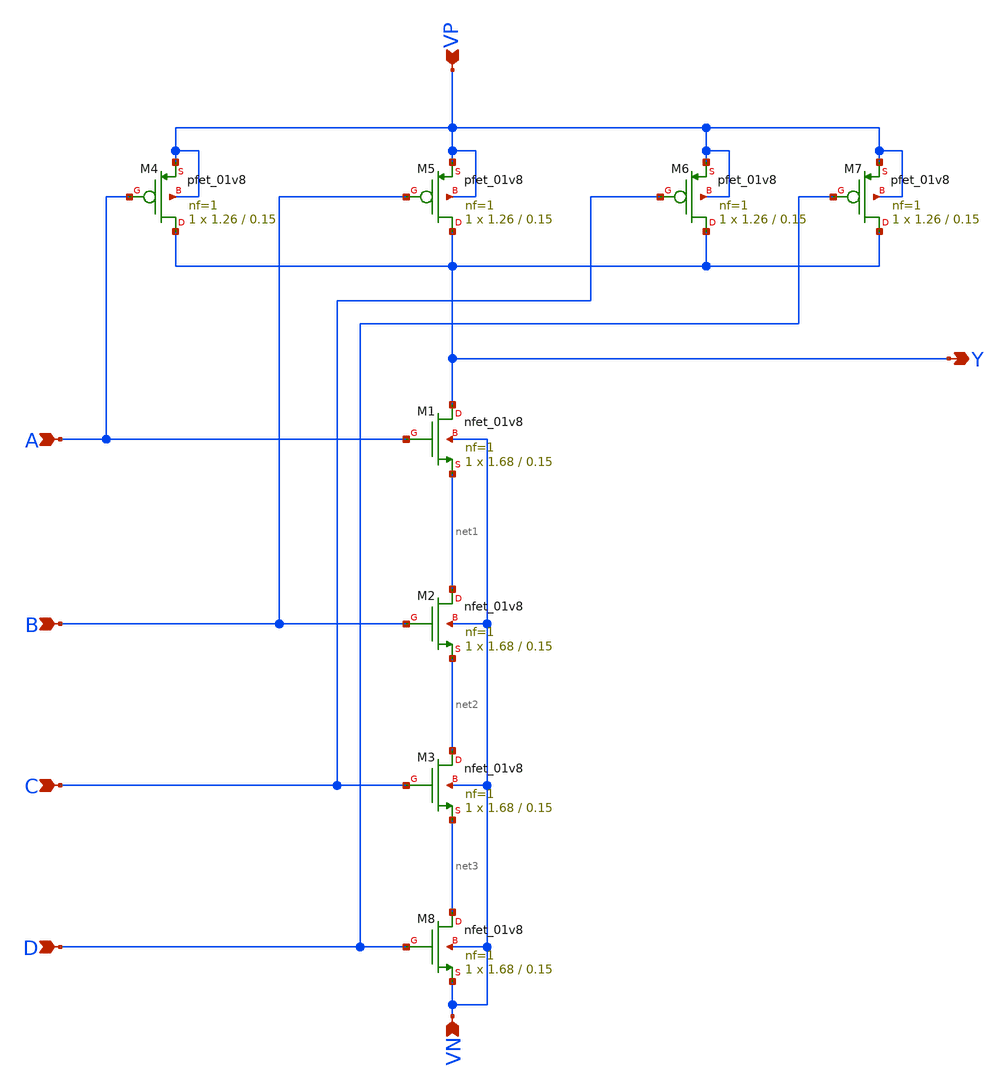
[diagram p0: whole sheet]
** sch_path: component/NAND4/nand4.sch
**.subckt nand4 A B C Y D VP VN
*.ipin A
*.ipin B
*.ipin C
*.opin Y
*.ipin D
*.ipin VP
*.ipin VN
XM1 Y A net1 VN sky130_fd_pr__nfet_01v8 L=0.15 W=1.68 nf=1 ad='int((nf+1)/2) * W/nf * 0.29' as='int((nf+2)/2) * W/nf * 0.29'
+ pd='2*int((nf+1)/2) * (W/nf + 0.29)' ps='2*int((nf+2)/2) * (W/nf + 0.29)' nrd='0.29 / W' nrs='0.29 / W'
+ sa=0 sb=0 sd=0 mult=1 m=1
XM2 net1 B net2 VN sky130_fd_pr__nfet_01v8 L=0.15 W=1.68 nf=1 ad='int((nf+1)/2) * W/nf * 0.29' as='int((nf+2)/2) * W/nf * 0.29'
+ pd='2*int((nf+1)/2) * (W/nf + 0.29)' ps='2*int((nf+2)/2) * (W/nf + 0.29)' nrd='0.29 / W' nrs='0.29 / W'
+ sa=0 sb=0 sd=0 mult=1 m=1
XM3 net2 C net3 VN sky130_fd_pr__nfet_01v8 L=0.15 W=1.68 nf=1 ad='int((nf+1)/2) * W/nf * 0.29' as='int((nf+2)/2) * W/nf * 0.29'
+ pd='2*int((nf+1)/2) * (W/nf + 0.29)' ps='2*int((nf+2)/2) * (W/nf + 0.29)' nrd='0.29 / W' nrs='0.29 / W'
+ sa=0 sb=0 sd=0 mult=1 m=1
XM4 Y A VP VP sky130_fd_pr__pfet_01v8 L=0.15 W=1.26 nf=1 ad='int((nf+1)/2) * W/nf * 0.29' as='int((nf+2)/2) * W/nf * 0.29'
+ pd='2*int((nf+1)/2) * (W/nf + 0.29)' ps='2*int((nf+2)/2) * (W/nf + 0.29)' nrd='0.29 / W' nrs='0.29 / W'
+ sa=0 sb=0 sd=0 mult=1 m=1
XM5 Y B VP VP sky130_fd_pr__pfet_01v8 L=0.15 W=1.26 nf=1 ad='int((nf+1)/2) * W/nf * 0.29' as='int((nf+2)/2) * W/nf * 0.29'
+ pd='2*int((nf+1)/2) * (W/nf + 0.29)' ps='2*int((nf+2)/2) * (W/nf + 0.29)' nrd='0.29 / W' nrs='0.29 / W'
+ sa=0 sb=0 sd=0 mult=1 m=1
XM6 Y C VP VP sky130_fd_pr__pfet_01v8 L=0.15 W=1.26 nf=1 ad='int((nf+1)/2) * W/nf * 0.29' as='int((nf+2)/2) * W/nf * 0.29'
+ pd='2*int((nf+1)/2) * (W/nf + 0.29)' ps='2*int((nf+2)/2) * (W/nf + 0.29)' nrd='0.29 / W' nrs='0.29 / W'
+ sa=0 sb=0 sd=0 mult=1 m=1
XM7 Y D VP VP sky130_fd_pr__pfet_01v8 L=0.15 W=1.26 nf=1 ad='int((nf+1)/2) * W/nf * 0.29' as='int((nf+2)/2) * W/nf * 0.29'
+ pd='2*int((nf+1)/2) * (W/nf + 0.29)' ps='2*int((nf+2)/2) * (W/nf + 0.29)' nrd='0.29 / W' nrs='0.29 / W'
+ sa=0 sb=0 sd=0 mult=1 m=1
XM8 net3 D VN VN sky130_fd_pr__nfet_01v8 L=0.15 W=1.68 nf=1 ad='int((nf+1)/2) * W/nf * 0.29' as='int((nf+2)/2) * W/nf * 0.29'
+ pd='2*int((nf+1)/2) * (W/nf + 0.29)' ps='2*int((nf+2)/2) * (W/nf + 0.29)' nrd='0.29 / W' nrs='0.29 / W'
+ sa=0 sb=0 sd=0 mult=1 m=1
**.ends
.end
